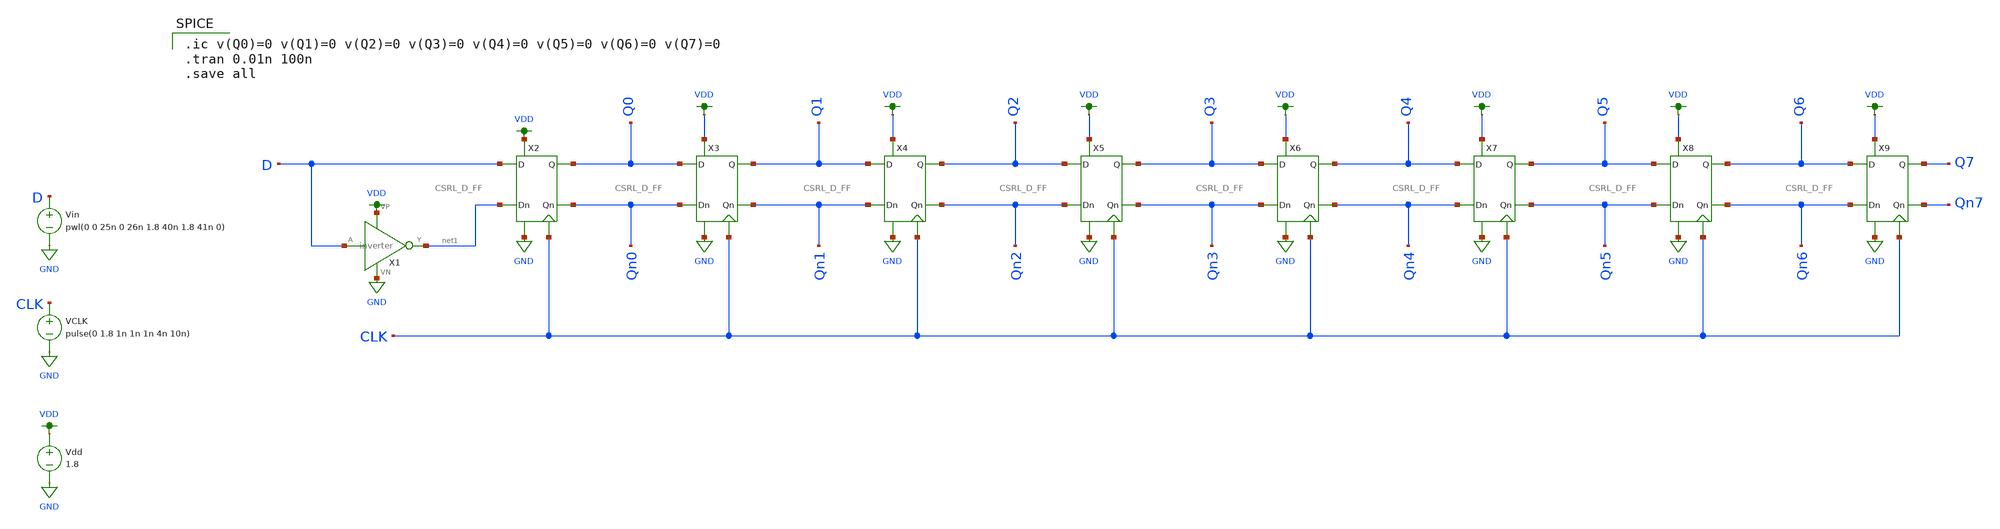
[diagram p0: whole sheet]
** sch_path: schematic/shift-register-8-bit.sch
**.subckt shift-register-8-bit
Vin D GND pwl(0 0 25n 0 26n 1.8 40n 1.8 41n 0)
VCLK CLK GND pulse(0 1.8 1n 1n 1n 4n 10n)
Vdd VDD GND 1.8
X1 D net1 VDD GND inverter
X2 net1 D Qn0 Q0 GND VDD CLK CSRL_D_FF
X3 Qn0 Q0 Qn1 Q1 GND VDD CLK CSRL_D_FF
X4 Qn1 Q1 Qn2 Q2 GND VDD CLK CSRL_D_FF
X5 Qn2 Q2 Qn3 Q3 GND VDD CLK CSRL_D_FF
X6 Qn3 Q3 Qn4 Q4 GND VDD CLK CSRL_D_FF
X7 Qn4 Q4 Qn5 Q5 GND VDD CLK CSRL_D_FF
X8 Qn5 Q5 Qn6 Q6 GND VDD CLK CSRL_D_FF
X9 Qn6 Q6 Qn7 Q7 GND VDD CLK CSRL_D_FF
**** begin user architecture code

.ic v(Q0)=0 v(Q1)=0 v(Q2)=0 v(Q3)=0 v(Q4)=0 v(Q5)=0 v(Q6)=0 v(Q7)=0
.tran 0.01n 100n
.save all


.option wnflag=1
.param MC_SWITCH=0.0
.lib ~/skywater/skywater-pdk/libraries/sky130_fd_pr_ngspice/latest/models/sky130.lib.spice tt

**** end user architecture code
**.ends

* expanding   symbol:  /home/madvlsi/Documents/MADVLSI-Final_Project/schematic/inverter.sym # of
*+ pins=4
** sym_path: schematic/inverter.sym
** sch_path: schematic/inverter.sch
.subckt inverter A Y VP VN
*.opin Y
*.ipin A
*.iopin VP
*.iopin VN
XM3 Y A VP VDD sky130_fd_pr__pfet_01v8 L={Lp} W={Wp} nf=1 ad='int((nf+1)/2) * W/nf * 0.29' as='int((nf+2)/2) * W/nf * 0.29'
+ pd='2*int((nf+1)/2) * (W/nf + 0.29)' ps='2*int((nf+2)/2) * (W/nf + 0.29)' nrd='0.29 / W' nrs='0.29 / W'
+ sa=0 sb=0 sd=0 mult=1 m=1
XM4 Y A VP VDD sky130_fd_pr__pfet_01v8 L={Lp} W={Wp} nf=1 ad='int((nf+1)/2) * W/nf * 0.29' as='int((nf+2)/2) * W/nf * 0.29'
+ pd='2*int((nf+1)/2) * (W/nf + 0.29)' ps='2*int((nf+2)/2) * (W/nf + 0.29)' nrd='0.29 / W' nrs='0.29 / W'
+ sa=0 sb=0 sd=0 mult=1 m=1
XM5 Y A VN GND sky130_fd_pr__nfet_01v8 L={Lp} W={Wp} nf=1 ad='int((nf+1)/2) * W/nf * 0.29' as='int((nf+2)/2) * W/nf * 0.29'
+ pd='2*int((nf+1)/2) * (W/nf + 0.29)' ps='2*int((nf+2)/2) * (W/nf + 0.29)' nrd='0.29 / W' nrs='0.29 / W'
+ sa=0 sb=0 sd=0 mult=1 m=1
.ends


* expanding   symbol:  /home/madvlsi/Documents/MADVLSI-Final_Project/schematic/CSRL_D_FF.sym # of
*+ pins=7
** sym_path: schematic/CSRL_D_FF.sym
** sch_path: schematic/CSRL_D_FF.sch
.subckt CSRL_D_FF Dn D Qn Q VN VP CLK
*.ipin Dn
*.ipin D
*.iopin VP
*.iopin VN
*.iopin CLK
*.opin Qn
*.opin Q
XM1 net5 CLK VP VDD sky130_fd_pr__pfet_01v8 L=0.15 W=1 nf=1 ad='int((nf+1)/2) * W/nf * 0.29' as='int((nf+2)/2) * W/nf * 0.29'
+ pd='2*int((nf+1)/2) * (W/nf + 0.29)' ps='2*int((nf+2)/2) * (W/nf + 0.29)' nrd='0.29 / W' nrs='0.29 / W'
+ sa=0 sb=0 sd=0 mult=1 m=1
XM2 net6 CLK VP VDD sky130_fd_pr__pfet_01v8 L=0.15 W=1 nf=1 ad='int((nf+1)/2) * W/nf * 0.29' as='int((nf+2)/2) * W/nf * 0.29'
+ pd='2*int((nf+1)/2) * (W/nf + 0.29)' ps='2*int((nf+2)/2) * (W/nf + 0.29)' nrd='0.29 / W' nrs='0.29 / W'
+ sa=0 sb=0 sd=0 mult=1 m=1
XM3 net3 CLK Q GND sky130_fd_pr__nfet_01v8 L=0.15 W=1 nf=1 ad='int((nf+1)/2) * W/nf * 0.29' as='int((nf+2)/2) * W/nf * 0.29'
+ pd='2*int((nf+1)/2) * (W/nf + 0.29)' ps='2*int((nf+2)/2) * (W/nf + 0.29)' nrd='0.29 / W' nrs='0.29 / W'
+ sa=0 sb=0 sd=0 mult=1 m=1
XM4 net4 CLK Qn GND sky130_fd_pr__nfet_01v8 L=0.15 W=1 nf=1 ad='int((nf+1)/2) * W/nf * 0.29' as='int((nf+2)/2) * W/nf * 0.29'
+ pd='2*int((nf+1)/2) * (W/nf + 0.29)' ps='2*int((nf+2)/2) * (W/nf + 0.29)' nrd='0.29 / W' nrs='0.29 / W'
+ sa=0 sb=0 sd=0 mult=1 m=1
XM5 Q Qn net6 VDD sky130_fd_pr__pfet_01v8 L=0.15 W=1 nf=1 ad='int((nf+1)/2) * W/nf * 0.29' as='int((nf+2)/2) * W/nf * 0.29'
+ pd='2*int((nf+1)/2) * (W/nf + 0.29)' ps='2*int((nf+2)/2) * (W/nf + 0.29)' nrd='0.29 / W' nrs='0.29 / W'
+ sa=0 sb=0 sd=0 mult=1 m=1
XM6 VN Qn Q GND sky130_fd_pr__nfet_01v8 L=0.15 W=1 nf=1 ad='int((nf+1)/2) * W/nf * 0.29' as='int((nf+2)/2) * W/nf * 0.29'
+ pd='2*int((nf+1)/2) * (W/nf + 0.29)' ps='2*int((nf+2)/2) * (W/nf + 0.29)' nrd='0.29 / W' nrs='0.29 / W'
+ sa=0 sb=0 sd=0 mult=1 m=1
XM7 Qn Q net5 VDD sky130_fd_pr__pfet_01v8 L=0.15 W=1 nf=1 ad='int((nf+1)/2) * W/nf * 0.29' as='int((nf+2)/2) * W/nf * 0.29'
+ pd='2*int((nf+1)/2) * (W/nf + 0.29)' ps='2*int((nf+2)/2) * (W/nf + 0.29)' nrd='0.29 / W' nrs='0.29 / W'
+ sa=0 sb=0 sd=0 mult=1 m=1
XM8 VN Q Qn GND sky130_fd_pr__nfet_01v8 L=0.15 W=1 nf=1 ad='int((nf+1)/2) * W/nf * 0.29' as='int((nf+2)/2) * W/nf * 0.29'
+ pd='2*int((nf+1)/2) * (W/nf + 0.29)' ps='2*int((nf+2)/2) * (W/nf + 0.29)' nrd='0.29 / W' nrs='0.29 / W'
+ sa=0 sb=0 sd=0 mult=1 m=1
XM9 net4 CLK Dn VDD sky130_fd_pr__pfet_01v8 L=0.15 W=1 nf=1 ad='int((nf+1)/2) * W/nf * 0.29' as='int((nf+2)/2) * W/nf * 0.29'
+ pd='2*int((nf+1)/2) * (W/nf + 0.29)' ps='2*int((nf+2)/2) * (W/nf + 0.29)' nrd='0.29 / W' nrs='0.29 / W'
+ sa=0 sb=0 sd=0 mult=1 m=1
XM10 net3 CLK D VDD sky130_fd_pr__pfet_01v8 L=0.15 W=1 nf=1 ad='int((nf+1)/2) * W/nf * 0.29' as='int((nf+2)/2) * W/nf * 0.29'
+ pd='2*int((nf+1)/2) * (W/nf + 0.29)' ps='2*int((nf+2)/2) * (W/nf + 0.29)' nrd='0.29 / W' nrs='0.29 / W'
+ sa=0 sb=0 sd=0 mult=1 m=1
XM11 VN CLK net1 GND sky130_fd_pr__nfet_01v8 L=0.15 W=1 nf=1 ad='int((nf+1)/2) * W/nf * 0.29' as='int((nf+2)/2) * W/nf * 0.29'
+ pd='2*int((nf+1)/2) * (W/nf + 0.29)' ps='2*int((nf+2)/2) * (W/nf + 0.29)' nrd='0.29 / W' nrs='0.29 / W'
+ sa=0 sb=0 sd=0 mult=1 m=1
XM12 VN CLK net2 GND sky130_fd_pr__nfet_01v8 L=0.15 W=1 nf=1 ad='int((nf+1)/2) * W/nf * 0.29' as='int((nf+2)/2) * W/nf * 0.29'
+ pd='2*int((nf+1)/2) * (W/nf + 0.29)' ps='2*int((nf+2)/2) * (W/nf + 0.29)' nrd='0.29 / W' nrs='0.29 / W'
+ sa=0 sb=0 sd=0 mult=1 m=1
XM13 VP net3 net4 VDD sky130_fd_pr__pfet_01v8 L=0.15 W=1 nf=1 ad='int((nf+1)/2) * W/nf * 0.29' as='int((nf+2)/2) * W/nf * 0.29'
+ pd='2*int((nf+1)/2) * (W/nf + 0.29)' ps='2*int((nf+2)/2) * (W/nf + 0.29)' nrd='0.29 / W' nrs='0.29 / W'
+ sa=0 sb=0 sd=0 mult=1 m=1
XM14 VP net4 net3 VDD sky130_fd_pr__pfet_01v8 L=0.15 W=1 nf=1 ad='int((nf+1)/2) * W/nf * 0.29' as='int((nf+2)/2) * W/nf * 0.29'
+ pd='2*int((nf+1)/2) * (W/nf + 0.29)' ps='2*int((nf+2)/2) * (W/nf + 0.29)' nrd='0.29 / W' nrs='0.29 / W'
+ sa=0 sb=0 sd=0 mult=1 m=1
XM15 net3 net4 net1 GND sky130_fd_pr__nfet_01v8 L=0.15 W=1 nf=1 ad='int((nf+1)/2) * W/nf * 0.29' as='int((nf+2)/2) * W/nf * 0.29'
+ pd='2*int((nf+1)/2) * (W/nf + 0.29)' ps='2*int((nf+2)/2) * (W/nf + 0.29)' nrd='0.29 / W' nrs='0.29 / W'
+ sa=0 sb=0 sd=0 mult=1 m=1
XM16 net4 net3 net2 GND sky130_fd_pr__nfet_01v8 L=0.15 W=1 nf=1 ad='int((nf+1)/2) * W/nf * 0.29' as='int((nf+2)/2) * W/nf * 0.29'
+ pd='2*int((nf+1)/2) * (W/nf + 0.29)' ps='2*int((nf+2)/2) * (W/nf + 0.29)' nrd='0.29 / W' nrs='0.29 / W'
+ sa=0 sb=0 sd=0 mult=1 m=1
XM17 VN CLK net2 GND sky130_fd_pr__nfet_01v8 L=0.15 W=1 nf=1 ad='int((nf+1)/2) * W/nf * 0.29' as='int((nf+2)/2) * W/nf * 0.29'
+ pd='2*int((nf+1)/2) * (W/nf + 0.29)' ps='2*int((nf+2)/2) * (W/nf + 0.29)' nrd='0.29 / W' nrs='0.29 / W'
+ sa=0 sb=0 sd=0 mult=1 m=1
XM18 VN CLK net1 GND sky130_fd_pr__nfet_01v8 L=0.15 W=1 nf=1 ad='int((nf+1)/2) * W/nf * 0.29' as='int((nf+2)/2) * W/nf * 0.29'
+ pd='2*int((nf+1)/2) * (W/nf + 0.29)' ps='2*int((nf+2)/2) * (W/nf + 0.29)' nrd='0.29 / W' nrs='0.29 / W'
+ sa=0 sb=0 sd=0 mult=1 m=1
.ends

.GLOBAL GND
.GLOBAL VDD
.end
